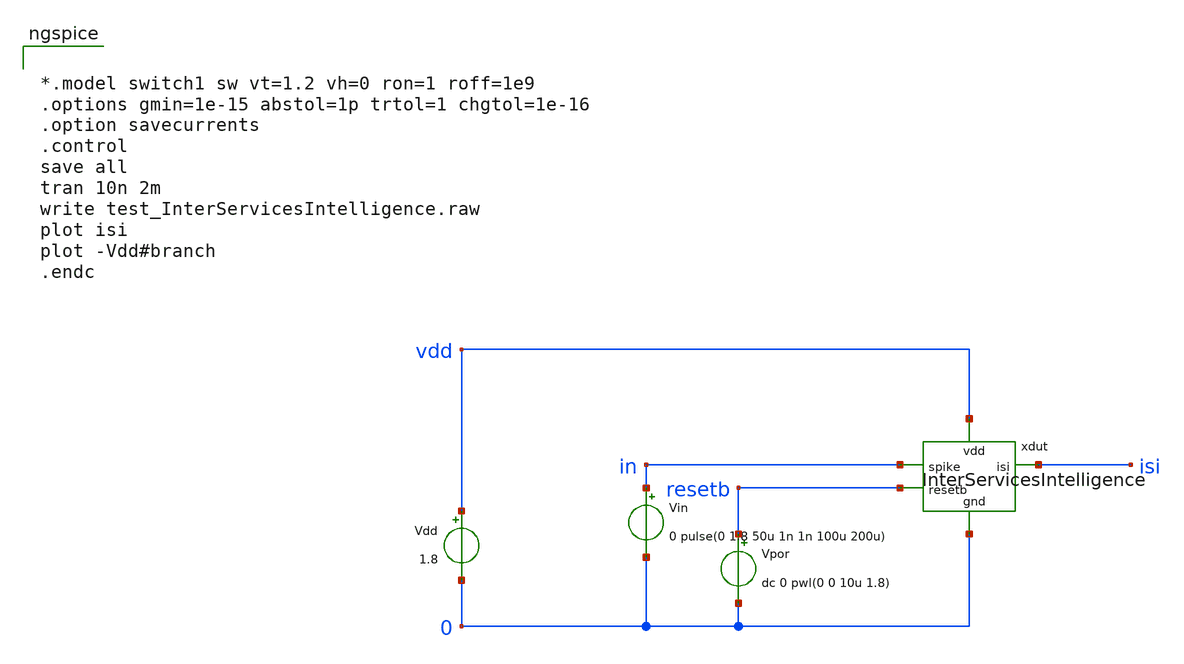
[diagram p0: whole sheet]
** sch_path: playground/test_InterServicesIntelligence.sch
* Copyright 2020 Stefan Frederik Schippers
* Licensed under the Apache License, Version 2.0 (the "License");
* you may not use this file except in compliance with the License.
* You may obtain a copy of the License at
* https://www.apache.org/licenses/LICENSE-2.0
* Unless required by applicable law or agreed to in writing, software
* distributed under the License is distributed on an "AS IS" BASIS,
* WITHOUT WARRANTIES OR CONDITIONS OF ANY KIND, either express or implied.
* See the License for the specific language governing permissions and
* limitations under the License.
**.subckt test_InterServicesIntelligence
Vdd vdd 0 1.8
Vin in 0 0 pulse(0 1.8 50u 1n 1n 100u 200u)
Vpor resetb 0 dc 0 pwl(0 0 10u 1.8)
xdut isi resetb vdd in 0 InterServicesIntelligence
**** begin user architecture code


*.model switch1 sw vt=1.2 vh=0 ron=1 roff=1e9
.options gmin=1e-15 abstol=1p trtol=1 chgtol=1e-16
.option savecurrents
.control
save all
tran 10n 2m
write test_InterServicesIntelligence.raw
plot isi
plot -Vdd#branch
.endc


 .lib $::SKYWATER_MODELS/models/sky130.lib.spice tt

.param mc_mm_switch=0
.param mc_pr_switch=1


**** end user architecture code
**.ends
.end
